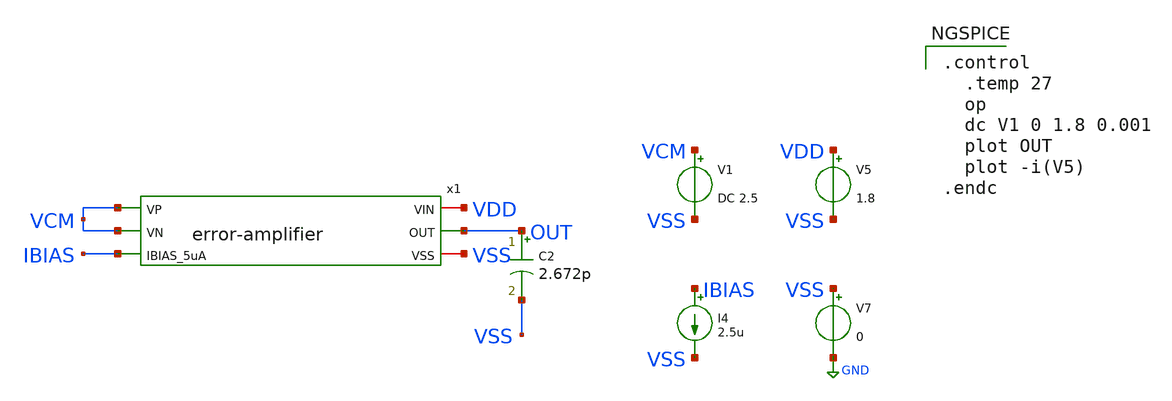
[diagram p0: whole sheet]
** sch_path: xschem/error-amplifier/testbench/tb_dc.sch
**.subckt tb_dc
C2 OUT VSS 2.672p m=1
V5 VDD VSS 1.8
V7 VSS GND 0
I4 IBIAS VSS 2.5u
V1 VCM VSS DC 2.5
x1 VDD VCM VCM IBIAS OUT VSS error-amplifier
**** begin user architecture code

.control
  .temp 27
  op
  dc V1 0 1.8 0.001
  plot OUT
  plot -i(V5)
.endc




** opencircuitdesign pdks install
.lib $::SKYWATER_MODELS/sky130.lib.spice tt


**** end user architecture code
**.ends

* expanding   symbol:
*+  /foss/designs/2026/tt_sky26b_ldo_andriansyah/xschem/error-amplifier/error-amplifier.sym # of pins=6
** sym_path: xschem/error-amplifier/error-amplifier.sym
** sch_path: xschem/error-amplifier/error-amplifier.sch
.subckt error-amplifier VIN VP VN IBIAS_5uA OUT VSS
*.ipin IBIAS_5uA
*.ipin VN
*.ipin VP
*.iopin VIN
*.iopin VSS
*.opin OUT
XM1 net2 net2 VSS VSS sky130_fd_pr__nfet_01v8 L=0.6 W=4.2 nf=4 ad='int((nf+1)/2) * W/nf * 0.29' as='int((nf+2)/2) * W/nf * 0.29'
+ pd='2*int((nf+1)/2) * (W/nf + 0.29)' ps='2*int((nf+2)/2) * (W/nf + 0.29)' nrd='0.29 / W' nrs='0.29 / W'
+ sa=0 sb=0 sd=0 mult=1 m=1
XM2 OUT net2 VSS VSS sky130_fd_pr__nfet_01v8 L=0.6 W=4.2 nf=4 ad='int((nf+1)/2) * W/nf * 0.29' as='int((nf+2)/2) * W/nf * 0.29'
+ pd='2*int((nf+1)/2) * (W/nf + 0.29)' ps='2*int((nf+2)/2) * (W/nf + 0.29)' nrd='0.29 / W' nrs='0.29 / W'
+ sa=0 sb=0 sd=0 mult=1 m=1
XM3 net2 VN net1 VDD sky130_fd_pr__pfet_01v8 L=0.6 W=28 nf=4 ad='int((nf+1)/2) * W/nf * 0.29' as='int((nf+2)/2) * W/nf * 0.29'
+ pd='2*int((nf+1)/2) * (W/nf + 0.29)' ps='2*int((nf+2)/2) * (W/nf + 0.29)' nrd='0.29 / W' nrs='0.29 / W'
+ sa=0 sb=0 sd=0 mult=1 m=1
XM4 OUT VP net1 VDD sky130_fd_pr__pfet_01v8 L=0.6 W=28 nf=4 ad='int((nf+1)/2) * W/nf * 0.29' as='int((nf+2)/2) * W/nf * 0.29'
+ pd='2*int((nf+1)/2) * (W/nf + 0.29)' ps='2*int((nf+2)/2) * (W/nf + 0.29)' nrd='0.29 / W' nrs='0.29 / W'
+ sa=0 sb=0 sd=0 mult=1 m=1
XM5 net1 IBIAS_5uA VIN VIN sky130_fd_pr__pfet_01v8 L=0.6 W=6.6 nf=4 ad='int((nf+1)/2) * W/nf * 0.29'
+ as='int((nf+2)/2) * W/nf * 0.29' pd='2*int((nf+1)/2) * (W/nf + 0.29)' ps='2*int((nf+2)/2) * (W/nf + 0.29)'
+ nrd='0.29 / W' nrs='0.29 / W' sa=0 sb=0 sd=0 mult=1 m=1
XM6 IBIAS_5uA IBIAS_5uA VIN VIN sky130_fd_pr__pfet_01v8 L=0.6 W=6.6 nf=4 ad='int((nf+1)/2) * W/nf * 0.29'
+ as='int((nf+2)/2) * W/nf * 0.29' pd='2*int((nf+1)/2) * (W/nf + 0.29)' ps='2*int((nf+2)/2) * (W/nf + 0.29)'
+ nrd='0.29 / W' nrs='0.29 / W' sa=0 sb=0 sd=0 mult=1 m=1
XM7 VDD VDD VDD VDD sky130_fd_pr__pfet_01v8 L=0.6 W=7 nf=1 ad='int((nf+1)/2) * W/nf * 0.29' as='int((nf+2)/2) * W/nf * 0.29'
+ pd='2*int((nf+1)/2) * (W/nf + 0.29)' ps='2*int((nf+2)/2) * (W/nf + 0.29)' nrd='0.29 / W' nrs='0.29 / W'
+ sa=0 sb=0 sd=0 mult=1 m=1
XM8 VSS VSS VSS VSS sky130_fd_pr__nfet_01v8 L=0.6 W=1.05 nf=1 ad='int((nf+1)/2) * W/nf * 0.29' as='int((nf+2)/2) * W/nf * 0.29'
+ pd='2*int((nf+1)/2) * (W/nf + 0.29)' ps='2*int((nf+2)/2) * (W/nf + 0.29)' nrd='0.29 / W' nrs='0.29 / W'
+ sa=0 sb=0 sd=0 mult=1 m=1
XM9 VDD VDD VDD VDD sky130_fd_pr__pfet_01v8 L=0.6 W=1.65 nf=1 ad='int((nf+1)/2) * W/nf * 0.29' as='int((nf+2)/2) * W/nf * 0.29'
+ pd='2*int((nf+1)/2) * (W/nf + 0.29)' ps='2*int((nf+2)/2) * (W/nf + 0.29)' nrd='0.29 / W' nrs='0.29 / W'
+ sa=0 sb=0 sd=0 mult=1 m=1
XM10 VSS VSS VSS VSS sky130_fd_pr__nfet_01v8 L=0.6 W=1.05 nf=1 ad='int((nf+1)/2) * W/nf * 0.29' as='int((nf+2)/2) * W/nf * 0.29'
+ pd='2*int((nf+1)/2) * (W/nf + 0.29)' ps='2*int((nf+2)/2) * (W/nf + 0.29)' nrd='0.29 / W' nrs='0.29 / W'
+ sa=0 sb=0 sd=0 mult=1 m=1
XM11 VDD VDD VDD VDD sky130_fd_pr__pfet_01v8 L=0.6 W=7 nf=1 ad='int((nf+1)/2) * W/nf * 0.29' as='int((nf+2)/2) * W/nf * 0.29'
+ pd='2*int((nf+1)/2) * (W/nf + 0.29)' ps='2*int((nf+2)/2) * (W/nf + 0.29)' nrd='0.29 / W' nrs='0.29 / W'
+ sa=0 sb=0 sd=0 mult=1 m=1
XM12 VDD VDD VDD VDD sky130_fd_pr__pfet_01v8 L=0.6 W=1.65 nf=1 ad='int((nf+1)/2) * W/nf * 0.29' as='int((nf+2)/2) * W/nf * 0.29'
+ pd='2*int((nf+1)/2) * (W/nf + 0.29)' ps='2*int((nf+2)/2) * (W/nf + 0.29)' nrd='0.29 / W' nrs='0.29 / W'
+ sa=0 sb=0 sd=0 mult=1 m=1
.ends

.GLOBAL GND
.end
